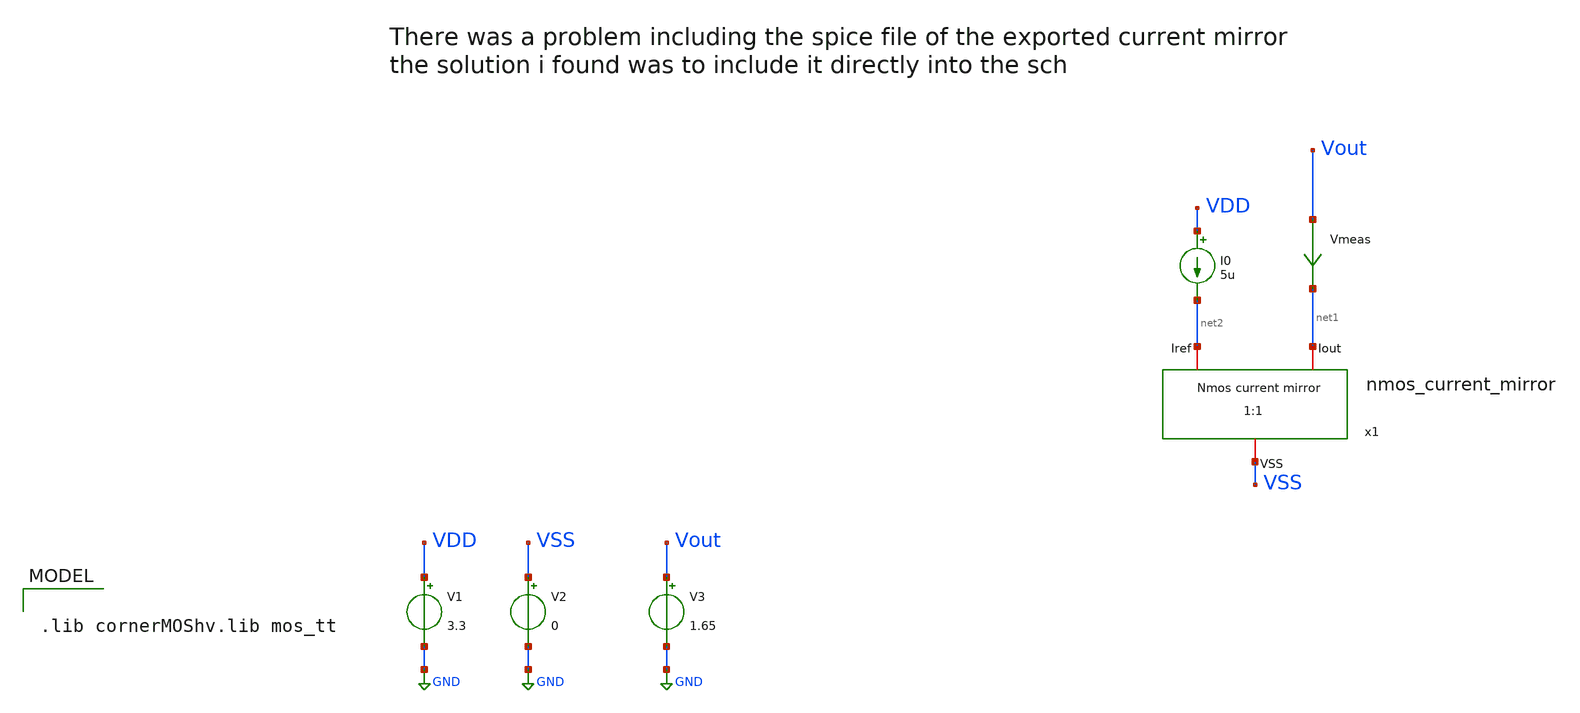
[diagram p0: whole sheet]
** sch_path: Learning/Current_mirrors/Design_nmos_current_mirror_ihp_3_3V/simulations/current_mirror_tb_.sch
**.subckt current_mirror_tb_
V1 VDD GND 3.3
V2 VSS GND 0
I0 VDD net2 5u
Vmeas Vout net1 0
.save i(vmeas)
V3 Vout GND 1.65
x1 VSS net2 net1 nmos_current_mirror
**** begin user architecture code

.lib cornerMOShv.lib mos_tt



.param temp=27
.param mm_ok=1
.param mc_ok=1
.control



save all
op
dc V3 0 3.3 0.001
plot i(Vmeas)
wrdata current_mirror.csv i(Vmeas)
.endc


* NGSPICE file created from TOP.ext - technology: ihp-sg13g2

.subckt nmos_current_mirror VSS Iref Iout
X0 VSS Iref Iout VSUB sg13_hv_nmos ad=0.34p pd=2.68u as=0.34p ps=2.68u w=1u l=2.2u
X1 Iout Iref VSS VSUB sg13_hv_nmos ad=0.47302p pd=5.005u as=40.72922p ps=0.14101m w=1u l=2.2u
X2 VSS Iref Iref VSUB sg13_hv_nmos ad=0 pd=0 as=12.88392p ps=59.825u w=1u l=2.2u
X3 Iref VSS VSS VSUB sg13_hv_nmos ad=0 pd=0 as=0 ps=0 w=1u l=2.2u
X4 VSS Iref Iref VSUB sg13_hv_nmos ad=0 pd=0 as=0 ps=0 w=1u l=2.2u
X5 Iref VSS VSS VSUB sg13_hv_nmos ad=0 pd=0 as=0 ps=0 w=1u l=2.2u
X6 VSS Iref Iout VSUB sg13_hv_nmos ad=0 pd=0 as=0 ps=0 w=1u l=2.2u
X7 Iout Iref VSS VSUB sg13_hv_nmos ad=0 pd=0 as=0 ps=0 w=1u l=2.2u
X8 Iref VSS VSS VSUB sg13_hv_nmos ad=0 pd=0 as=0 ps=0 w=1u l=2.2u
X9 VSS Iref Iref VSUB sg13_hv_nmos ad=0 pd=0 as=0 ps=0 w=1u l=2.2u
X10 VSS Iref Iref VSUB sg13_hv_nmos ad=0 pd=0 as=0 ps=0 w=1u l=2.2u
X11 Iref VSS VSS VSUB sg13_hv_nmos ad=0 pd=0 as=0 ps=0 w=1u l=2.2u
C0 VSS Iref 3.04697f
C1 Iref VSUB 5.47165f
C2 VSS VSUB 6.12918f
.ends




**** end user architecture code
**.ends
.GLOBAL GND
.end
